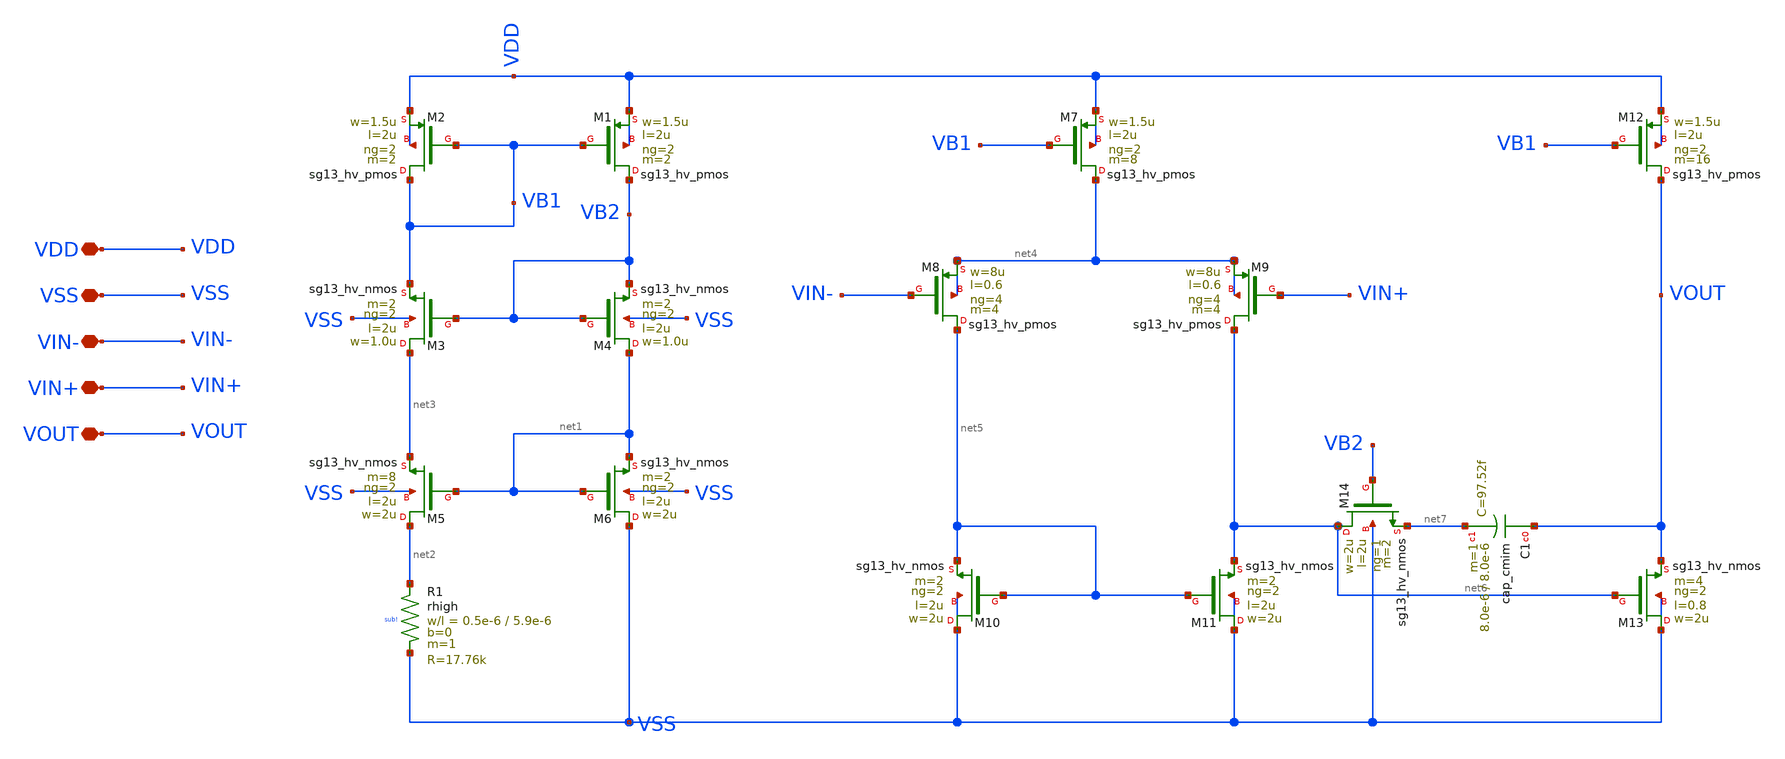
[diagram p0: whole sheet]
** sch_path: LIB/ihp-sg13g2/Amplifiers/Va001_ihp-sg13g2_3_3.sch
**.subckt Va001_ihp-sg13g2_3_3 VDD VSS VIN- VIN+ VOUT
*.iopin VDD
*.iopin VSS
*.iopin VIN-
*.iopin VIN+
*.iopin VOUT
XM2 VB1 VB1 VDD VDD sg13_hv_pmos w=1.5u l=2u ng=2 m=2 mm_ok=1
XM1 VB2 VB1 VDD VDD sg13_hv_pmos w=1.5u l=2u ng=2 m=2 mm_ok=1
XM3 net3 VB2 VB1 VSS sg13_hv_nmos w=1.0u l=2u ng=2 m=2 mm_ok=1
XM4 net1 VB2 VB2 VSS sg13_hv_nmos w=1.0u l=2u ng=2 m=2 mm_ok=1
XM5 net2 net1 net3 VSS sg13_hv_nmos w=2u l=2u ng=2 m=8 mm_ok=1
XM6 VSS net1 net1 VSS sg13_hv_nmos w=2u l=2u ng=2 m=2 mm_ok=1
XR1 net2 VSS sub! rhigh w=0.5e-6 l=5.9e-6 m=1 b=0 mm_ok=1
XM7 net4 VB1 VDD VDD sg13_hv_pmos w=1.5u l=2u ng=2 m=8 mm_ok=1
XM9 net6 VIN+ net4 net4 sg13_hv_pmos w=8u l=0.6 ng=4 m=4 mm_ok=1
XM8 net5 VIN- net4 net4 sg13_hv_pmos w=8u l=0.6 ng=4 m=4 mm_ok=1
XM10 VSS net5 net5 VSS sg13_hv_nmos w=2u l=2u ng=2 m=2 mm_ok=1
XM11 VSS net5 net6 VSS sg13_hv_nmos w=2u l=2u ng=2 m=2 mm_ok=1
XM12 VOUT VB1 VDD VDD sg13_hv_pmos w=1.5u l=2u ng=2 m=16 mm_ok=1
XM13 VSS net6 VOUT VSS sg13_hv_nmos w=2u l=0.8 ng=2 m=4 mm_ok=1
XM14 net6 VB2 net7 VSS sg13_hv_nmos w=2u l=2u ng=1 m=2 mm_ok=1
XC1 VOUT net7 cap_cmim w=8.0e-6 l=8.0e-6 m=1 mm_ok=1
**.ends
.end
